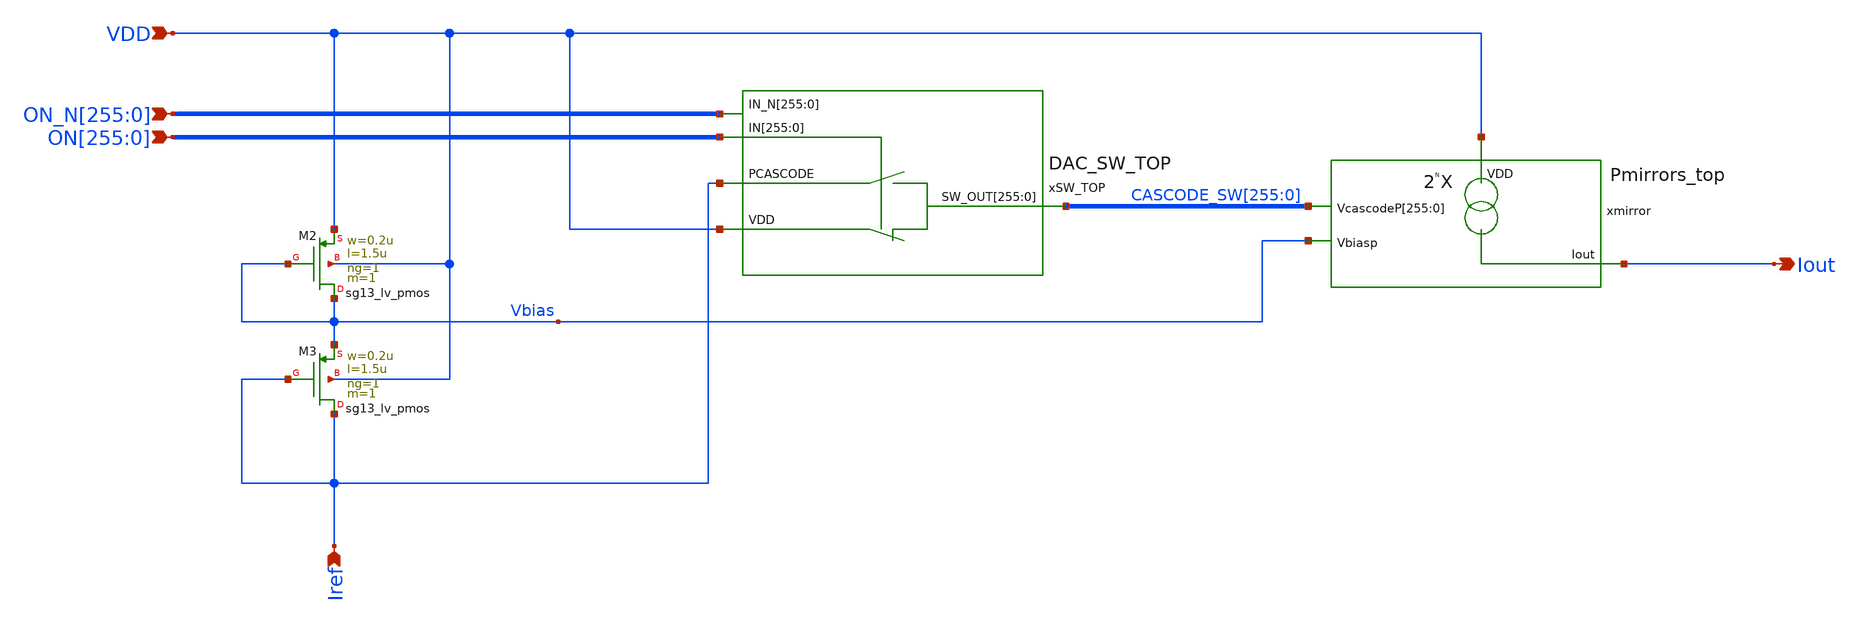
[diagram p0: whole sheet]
** sch_path: schematic/DAC_TOP.sch
**.subckt DAC_TOP VDD Iout
*+ ON[255],ON[254],ON[253],ON[252],ON[251],ON[250],ON[249],ON[248],ON[247],ON[246],ON[245],ON[244],ON[243],ON[242],ON[241],ON[240],ON[239],ON[238],ON[237],ON[236],ON[235],ON[234],ON[233],ON[232],ON[231],ON[230],ON[229],ON[228],ON[227],ON[226],ON[225],ON[224],ON[223],ON[222],ON[221],ON[220],ON[219],ON[218],ON[217],ON[216],ON[215],ON[214],ON[213],ON[212],ON[211],ON[210],ON[209],ON[208],ON[207],ON[206],ON[205],ON[204],ON[203],ON[202],ON[201],ON[200],ON[199],ON[198],ON[197],ON[196],ON[195],ON[194],ON[193],ON[192],ON[191],ON[190],ON[189],ON[188],ON[187],ON[186],ON[185],ON[184],ON[183],ON[182],ON[181],ON[180],ON[179],ON[178],ON[177],ON[176],ON[175],ON[174],ON[173],ON[172],ON[171],ON[170],ON[169],ON[168],ON[167],ON[166],ON[165],ON[164],ON[163],ON[162],ON[161],ON[160],ON[159],ON[158],ON[157],ON[156],ON[155],ON[154],ON[153],ON[152],ON[151],ON[150],ON[149],ON[148],ON[147],ON[146],ON[145],ON[144],ON[143],ON[142],ON[141],ON[140],ON[139],ON[138],ON[137],ON[136],ON[135],ON[134],ON[133],ON[132],ON[131],ON[130],ON[129],ON[128],ON[127],ON[126],ON[125],ON[124],ON[123],ON[122],ON[121],ON[120],ON[119],ON[118],ON[117],ON[116],ON[115],ON[114],ON[113],ON[112],ON[111],ON[110],ON[109],ON[108],ON[107],ON[106],ON[105],ON[104],ON[103],ON[102],ON[101],ON[100],ON[99],ON[98],ON[97],ON[96],ON[95],ON[94],ON[93],ON[92],ON[91],ON[90],ON[89],ON[88],ON[87],ON[86],ON[85],ON[84],ON[83],ON[82],ON[81],ON[80],ON[79],ON[78],ON[77],ON[76],ON[75],ON[74],ON[73],ON[72],ON[71],ON[70],ON[69],ON[68],ON[67],ON[66],ON[65],ON[64],ON[63],ON[62],ON[61],ON[60],ON[59],ON[58],ON[57],ON[56],ON[55],ON[54],ON[53],ON[52],ON[51],ON[50],ON[49],ON[48],ON[47],ON[46],ON[45],ON[44],ON[43],ON[42],ON[41],ON[40],ON[39],ON[38],ON[37],ON[36],ON[35],ON[34],ON[33],ON[32],ON[31],ON[30],ON[29],ON[28],ON[27],ON[26],ON[25],ON[24],ON[23],ON[22],ON[21],ON[20],ON[19],ON[18],ON[17],ON[16],ON[15],ON[14],ON[13],ON[12],ON[11],ON[10],ON[9],ON[8],ON[7],ON[6],ON[5],ON[4],ON[3],ON[2],ON[1],ON[0] Iref
*+ ON_N[255],ON_N[254],ON_N[253],ON_N[252],ON_N[251],ON_N[250],ON_N[249],ON_N[248],ON_N[247],ON_N[246],ON_N[245],ON_N[244],ON_N[243],ON_N[242],ON_N[241],ON_N[240],ON_N[239],ON_N[238],ON_N[237],ON_N[236],ON_N[235],ON_N[234],ON_N[233],ON_N[232],ON_N[231],ON_N[230],ON_N[229],ON_N[228],ON_N[227],ON_N[226],ON_N[225],ON_N[224],ON_N[223],ON_N[222],ON_N[221],ON_N[220],ON_N[219],ON_N[218],ON_N[217],ON_N[216],ON_N[215],ON_N[214],ON_N[213],ON_N[212],ON_N[211],ON_N[210],ON_N[209],ON_N[208],ON_N[207],ON_N[206],ON_N[205],ON_N[204],ON_N[203],ON_N[202],ON_N[201],ON_N[200],ON_N[199],ON_N[198],ON_N[197],ON_N[196],ON_N[195],ON_N[194],ON_N[193],ON_N[192],ON_N[191],ON_N[190],ON_N[189],ON_N[188],ON_N[187],ON_N[186],ON_N[185],ON_N[184],ON_N[183],ON_N[182],ON_N[181],ON_N[180],ON_N[179],ON_N[178],ON_N[177],ON_N[176],ON_N[175],ON_N[174],ON_N[173],ON_N[172],ON_N[171],ON_N[170],ON_N[169],ON_N[168],ON_N[167],ON_N[166],ON_N[165],ON_N[164],ON_N[163],ON_N[162],ON_N[161],ON_N[160],ON_N[159],ON_N[158],ON_N[157],ON_N[156],ON_N[155],ON_N[154],ON_N[153],ON_N[152],ON_N[151],ON_N[150],ON_N[149],ON_N[148],ON_N[147],ON_N[146],ON_N[145],ON_N[144],ON_N[143],ON_N[142],ON_N[141],ON_N[140],ON_N[139],ON_N[138],ON_N[137],ON_N[136],ON_N[135],ON_N[134],ON_N[133],ON_N[132],ON_N[131],ON_N[130],ON_N[129],ON_N[128],ON_N[127],ON_N[126],ON_N[125],ON_N[124],ON_N[123],ON_N[122],ON_N[121],ON_N[120],ON_N[119],ON_N[118],ON_N[117],ON_N[116],ON_N[115],ON_N[114],ON_N[113],ON_N[112],ON_N[111],ON_N[110],ON_N[109],ON_N[108],ON_N[107],ON_N[106],ON_N[105],ON_N[104],ON_N[103],ON_N[102],ON_N[101],ON_N[100],ON_N[99],ON_N[98],ON_N[97],ON_N[96],ON_N[95],ON_N[94],ON_N[93],ON_N[92],ON_N[91],ON_N[90],ON_N[89],ON_N[88],ON_N[87],ON_N[86],ON_N[85],ON_N[84],ON_N[83],ON_N[82],ON_N[81],ON_N[80],ON_N[79],ON_N[78],ON_N[77],ON_N[76],ON_N[75],ON_N[74],ON_N[73],ON_N[72],ON_N[71],ON_N[70],ON_N[69],ON_N[68],ON_N[67],ON_N[66],ON_N[65],ON_N[64],ON_N[63],ON_N[62],ON_N[61],ON_N[60],ON_N[59],ON_N[58],ON_N[57],ON_N[56],ON_N[55],ON_N[54],ON_N[53],ON_N[52],ON_N[51],ON_N[50],ON_N[49],ON_N[48],ON_N[47],ON_N[46],ON_N[45],ON_N[44],ON_N[43],ON_N[42],ON_N[41],ON_N[40],ON_N[39],ON_N[38],ON_N[37],ON_N[36],ON_N[35],ON_N[34],ON_N[33],ON_N[32],ON_N[31],ON_N[30],ON_N[29],ON_N[28],ON_N[27],ON_N[26],ON_N[25],ON_N[24],ON_N[23],ON_N[22],ON_N[21],ON_N[20],ON_N[19],ON_N[18],ON_N[17],ON_N[16],ON_N[15],ON_N[14],ON_N[13],ON_N[12],ON_N[11],ON_N[10],ON_N[9],ON_N[8],ON_N[7],ON_N[6],ON_N[5],ON_N[4],ON_N[3],ON_N[2],ON_N[1],ON_N[0]
*.ipin VDD
*.opin Iout
*.ipin
*+ ON[255],ON[254],ON[253],ON[252],ON[251],ON[250],ON[249],ON[248],ON[247],ON[246],ON[245],ON[244],ON[243],ON[242],ON[241],ON[240],ON[239],ON[238],ON[237],ON[236],ON[235],ON[234],ON[233],ON[232],ON[231],ON[230],ON[229],ON[228],ON[227],ON[226],ON[225],ON[224],ON[223],ON[222],ON[221],ON[220],ON[219],ON[218],ON[217],ON[216],ON[215],ON[214],ON[213],ON[212],ON[211],ON[210],ON[209],ON[208],ON[207],ON[206],ON[205],ON[204],ON[203],ON[202],ON[201],ON[200],ON[199],ON[198],ON[197],ON[196],ON[195],ON[194],ON[193],ON[192],ON[191],ON[190],ON[189],ON[188],ON[187],ON[186],ON[185],ON[184],ON[183],ON[182],ON[181],ON[180],ON[179],ON[178],ON[177],ON[176],ON[175],ON[174],ON[173],ON[172],ON[171],ON[170],ON[169],ON[168],ON[167],ON[166],ON[165],ON[164],ON[163],ON[162],ON[161],ON[160],ON[159],ON[158],ON[157],ON[156],ON[155],ON[154],ON[153],ON[152],ON[151],ON[150],ON[149],ON[148],ON[147],ON[146],ON[145],ON[144],ON[143],ON[142],ON[141],ON[140],ON[139],ON[138],ON[137],ON[136],ON[135],ON[134],ON[133],ON[132],ON[131],ON[130],ON[129],ON[128],ON[127],ON[126],ON[125],ON[124],ON[123],ON[122],ON[121],ON[120],ON[119],ON[118],ON[117],ON[116],ON[115],ON[114],ON[113],ON[112],ON[111],ON[110],ON[109],ON[108],ON[107],ON[106],ON[105],ON[104],ON[103],ON[102],ON[101],ON[100],ON[99],ON[98],ON[97],ON[96],ON[95],ON[94],ON[93],ON[92],ON[91],ON[90],ON[89],ON[88],ON[87],ON[86],ON[85],ON[84],ON[83],ON[82],ON[81],ON[80],ON[79],ON[78],ON[77],ON[76],ON[75],ON[74],ON[73],ON[72],ON[71],ON[70],ON[69],ON[68],ON[67],ON[66],ON[65],ON[64],ON[63],ON[62],ON[61],ON[60],ON[59],ON[58],ON[57],ON[56],ON[55],ON[54],ON[53],ON[52],ON[51],ON[50],ON[49],ON[48],ON[47],ON[46],ON[45],ON[44],ON[43],ON[42],ON[41],ON[40],ON[39],ON[38],ON[37],ON[36],ON[35],ON[34],ON[33],ON[32],ON[31],ON[30],ON[29],ON[28],ON[27],ON[26],ON[25],ON[24],ON[23],ON[22],ON[21],ON[20],ON[19],ON[18],ON[17],ON[16],ON[15],ON[14],ON[13],ON[12],ON[11],ON[10],ON[9],ON[8],ON[7],ON[6],ON[5],ON[4],ON[3],ON[2],ON[1],ON[0]
*.ipin Iref
*.ipin
*+ ON_N[255],ON_N[254],ON_N[253],ON_N[252],ON_N[251],ON_N[250],ON_N[249],ON_N[248],ON_N[247],ON_N[246],ON_N[245],ON_N[244],ON_N[243],ON_N[242],ON_N[241],ON_N[240],ON_N[239],ON_N[238],ON_N[237],ON_N[236],ON_N[235],ON_N[234],ON_N[233],ON_N[232],ON_N[231],ON_N[230],ON_N[229],ON_N[228],ON_N[227],ON_N[226],ON_N[225],ON_N[224],ON_N[223],ON_N[222],ON_N[221],ON_N[220],ON_N[219],ON_N[218],ON_N[217],ON_N[216],ON_N[215],ON_N[214],ON_N[213],ON_N[212],ON_N[211],ON_N[210],ON_N[209],ON_N[208],ON_N[207],ON_N[206],ON_N[205],ON_N[204],ON_N[203],ON_N[202],ON_N[201],ON_N[200],ON_N[199],ON_N[198],ON_N[197],ON_N[196],ON_N[195],ON_N[194],ON_N[193],ON_N[192],ON_N[191],ON_N[190],ON_N[189],ON_N[188],ON_N[187],ON_N[186],ON_N[185],ON_N[184],ON_N[183],ON_N[182],ON_N[181],ON_N[180],ON_N[179],ON_N[178],ON_N[177],ON_N[176],ON_N[175],ON_N[174],ON_N[173],ON_N[172],ON_N[171],ON_N[170],ON_N[169],ON_N[168],ON_N[167],ON_N[166],ON_N[165],ON_N[164],ON_N[163],ON_N[162],ON_N[161],ON_N[160],ON_N[159],ON_N[158],ON_N[157],ON_N[156],ON_N[155],ON_N[154],ON_N[153],ON_N[152],ON_N[151],ON_N[150],ON_N[149],ON_N[148],ON_N[147],ON_N[146],ON_N[145],ON_N[144],ON_N[143],ON_N[142],ON_N[141],ON_N[140],ON_N[139],ON_N[138],ON_N[137],ON_N[136],ON_N[135],ON_N[134],ON_N[133],ON_N[132],ON_N[131],ON_N[130],ON_N[129],ON_N[128],ON_N[127],ON_N[126],ON_N[125],ON_N[124],ON_N[123],ON_N[122],ON_N[121],ON_N[120],ON_N[119],ON_N[118],ON_N[117],ON_N[116],ON_N[115],ON_N[114],ON_N[113],ON_N[112],ON_N[111],ON_N[110],ON_N[109],ON_N[108],ON_N[107],ON_N[106],ON_N[105],ON_N[104],ON_N[103],ON_N[102],ON_N[101],ON_N[100],ON_N[99],ON_N[98],ON_N[97],ON_N[96],ON_N[95],ON_N[94],ON_N[93],ON_N[92],ON_N[91],ON_N[90],ON_N[89],ON_N[88],ON_N[87],ON_N[86],ON_N[85],ON_N[84],ON_N[83],ON_N[82],ON_N[81],ON_N[80],ON_N[79],ON_N[78],ON_N[77],ON_N[76],ON_N[75],ON_N[74],ON_N[73],ON_N[72],ON_N[71],ON_N[70],ON_N[69],ON_N[68],ON_N[67],ON_N[66],ON_N[65],ON_N[64],ON_N[63],ON_N[62],ON_N[61],ON_N[60],ON_N[59],ON_N[58],ON_N[57],ON_N[56],ON_N[55],ON_N[54],ON_N[53],ON_N[52],ON_N[51],ON_N[50],ON_N[49],ON_N[48],ON_N[47],ON_N[46],ON_N[45],ON_N[44],ON_N[43],ON_N[42],ON_N[41],ON_N[40],ON_N[39],ON_N[38],ON_N[37],ON_N[36],ON_N[35],ON_N[34],ON_N[33],ON_N[32],ON_N[31],ON_N[30],ON_N[29],ON_N[28],ON_N[27],ON_N[26],ON_N[25],ON_N[24],ON_N[23],ON_N[22],ON_N[21],ON_N[20],ON_N[19],ON_N[18],ON_N[17],ON_N[16],ON_N[15],ON_N[14],ON_N[13],ON_N[12],ON_N[11],ON_N[10],ON_N[9],ON_N[8],ON_N[7],ON_N[6],ON_N[5],ON_N[4],ON_N[3],ON_N[2],ON_N[1],ON_N[0]
xmirror VDD Iout Vbias CASCODE_SW[255] CASCODE_SW[254] CASCODE_SW[253] CASCODE_SW[252]
+ CASCODE_SW[251] CASCODE_SW[250] CASCODE_SW[249] CASCODE_SW[248] CASCODE_SW[247] CASCODE_SW[246] CASCODE_SW[245]
+ CASCODE_SW[244] CASCODE_SW[243] CASCODE_SW[242] CASCODE_SW[241] CASCODE_SW[240] CASCODE_SW[239] CASCODE_SW[238]
+ CASCODE_SW[237] CASCODE_SW[236] CASCODE_SW[235] CASCODE_SW[234] CASCODE_SW[233] CASCODE_SW[232] CASCODE_SW[231]
+ CASCODE_SW[230] CASCODE_SW[229] CASCODE_SW[228] CASCODE_SW[227] CASCODE_SW[226] CASCODE_SW[225] CASCODE_SW[224]
+ CASCODE_SW[223] CASCODE_SW[222] CASCODE_SW[221] CASCODE_SW[220] CASCODE_SW[219] CASCODE_SW[218] CASCODE_SW[217]
+ CASCODE_SW[216] CASCODE_SW[215] CASCODE_SW[214] CASCODE_SW[213] CASCODE_SW[212] CASCODE_SW[211] CASCODE_SW[210]
+ CASCODE_SW[209] CASCODE_SW[208] CASCODE_SW[207] CASCODE_SW[206] CASCODE_SW[205] CASCODE_SW[204] CASCODE_SW[203]
+ CASCODE_SW[202] CASCODE_SW[201] CASCODE_SW[200] CASCODE_SW[199] CASCODE_SW[198] CASCODE_SW[197] CASCODE_SW[196]
+ CASCODE_SW[195] CASCODE_SW[194] CASCODE_SW[193] CASCODE_SW[192] CASCODE_SW[191] CASCODE_SW[190] CASCODE_SW[189]
+ CASCODE_SW[188] CASCODE_SW[187] CASCODE_SW[186] CASCODE_SW[185] CASCODE_SW[184] CASCODE_SW[183] CASCODE_SW[182]
+ CASCODE_SW[181] CASCODE_SW[180] CASCODE_SW[179] CASCODE_SW[178] CASCODE_SW[177] CASCODE_SW[176] CASCODE_SW[175]
+ CASCODE_SW[174] CASCODE_SW[173] CASCODE_SW[172] CASCODE_SW[171] CASCODE_SW[170] CASCODE_SW[169] CASCODE_SW[168]
+ CASCODE_SW[167] CASCODE_SW[166] CASCODE_SW[165] CASCODE_SW[164] CASCODE_SW[163] CASCODE_SW[162] CASCODE_SW[161]
+ CASCODE_SW[160] CASCODE_SW[159] CASCODE_SW[158] CASCODE_SW[157] CASCODE_SW[156] CASCODE_SW[155] CASCODE_SW[154]
+ CASCODE_SW[153] CASCODE_SW[152] CASCODE_SW[151] CASCODE_SW[150] CASCODE_SW[149] CASCODE_SW[148] CASCODE_SW[147]
+ CASCODE_SW[146] CASCODE_SW[145] CASCODE_SW[144] CASCODE_SW[143] CASCODE_SW[142] CASCODE_SW[141] CASCODE_SW[140]
+ CASCODE_SW[139] CASCODE_SW[138] CASCODE_SW[137] CASCODE_SW[136] CASCODE_SW[135] CASCODE_SW[134] CASCODE_SW[133]
+ CASCODE_SW[132] CASCODE_SW[131] CASCODE_SW[130] CASCODE_SW[129] CASCODE_SW[128] CASCODE_SW[127] CASCODE_SW[126]
+ CASCODE_SW[125] CASCODE_SW[124] CASCODE_SW[123] CASCODE_SW[122] CASCODE_SW[121] CASCODE_SW[120] CASCODE_SW[119]
+ CASCODE_SW[118] CASCODE_SW[117] CASCODE_SW[116] CASCODE_SW[115] CASCODE_SW[114] CASCODE_SW[113] CASCODE_SW[112]
+ CASCODE_SW[111] CASCODE_SW[110] CASCODE_SW[109] CASCODE_SW[108] CASCODE_SW[107] CASCODE_SW[106] CASCODE_SW[105]
+ CASCODE_SW[104] CASCODE_SW[103] CASCODE_SW[102] CASCODE_SW[101] CASCODE_SW[100] CASCODE_SW[99] CASCODE_SW[98]
+ CASCODE_SW[97] CASCODE_SW[96] CASCODE_SW[95] CASCODE_SW[94] CASCODE_SW[93] CASCODE_SW[92] CASCODE_SW[91]
+ CASCODE_SW[90] CASCODE_SW[89] CASCODE_SW[88] CASCODE_SW[87] CASCODE_SW[86] CASCODE_SW[85] CASCODE_SW[84]
+ CASCODE_SW[83] CASCODE_SW[82] CASCODE_SW[81] CASCODE_SW[80] CASCODE_SW[79] CASCODE_SW[78] CASCODE_SW[77]
+ CASCODE_SW[76] CASCODE_SW[75] CASCODE_SW[74] CASCODE_SW[73] CASCODE_SW[72] CASCODE_SW[71] CASCODE_SW[70]
+ CASCODE_SW[69] CASCODE_SW[68] CASCODE_SW[67] CASCODE_SW[66] CASCODE_SW[65] CASCODE_SW[64] CASCODE_SW[63]
+ CASCODE_SW[62] CASCODE_SW[61] CASCODE_SW[60] CASCODE_SW[59] CASCODE_SW[58] CASCODE_SW[57] CASCODE_SW[56]
+ CASCODE_SW[55] CASCODE_SW[54] CASCODE_SW[53] CASCODE_SW[52] CASCODE_SW[51] CASCODE_SW[50] CASCODE_SW[49]
+ CASCODE_SW[48] CASCODE_SW[47] CASCODE_SW[46] CASCODE_SW[45] CASCODE_SW[44] CASCODE_SW[43] CASCODE_SW[42]
+ CASCODE_SW[41] CASCODE_SW[40] CASCODE_SW[39] CASCODE_SW[38] CASCODE_SW[37] CASCODE_SW[36] CASCODE_SW[35]
+ CASCODE_SW[34] CASCODE_SW[33] CASCODE_SW[32] CASCODE_SW[31] CASCODE_SW[30] CASCODE_SW[29] CASCODE_SW[28]
+ CASCODE_SW[27] CASCODE_SW[26] CASCODE_SW[25] CASCODE_SW[24] CASCODE_SW[23] CASCODE_SW[22] CASCODE_SW[21]
+ CASCODE_SW[20] CASCODE_SW[19] CASCODE_SW[18] CASCODE_SW[17] CASCODE_SW[16] CASCODE_SW[15] CASCODE_SW[14]
+ CASCODE_SW[13] CASCODE_SW[12] CASCODE_SW[11] CASCODE_SW[10] CASCODE_SW[9] CASCODE_SW[8] CASCODE_SW[7]
+ CASCODE_SW[6] CASCODE_SW[5] CASCODE_SW[4] CASCODE_SW[3] CASCODE_SW[2] CASCODE_SW[1] CASCODE_SW[0] Pmirrors_top
XM2 Vbias Vbias VDD VDD sg13_lv_pmos w=0.2u l=1.5u ng=1 m=1 mm_ok=1
XM3 Iref Iref Vbias VDD sg13_lv_pmos w=0.2u l=1.5u ng=1 m=1 mm_ok=1
xSW_TOP Iref CASCODE_SW[255] CASCODE_SW[254] CASCODE_SW[253] CASCODE_SW[252] CASCODE_SW[251]
+ CASCODE_SW[250] CASCODE_SW[249] CASCODE_SW[248] CASCODE_SW[247] CASCODE_SW[246] CASCODE_SW[245] CASCODE_SW[244]
+ CASCODE_SW[243] CASCODE_SW[242] CASCODE_SW[241] CASCODE_SW[240] CASCODE_SW[239] CASCODE_SW[238] CASCODE_SW[237]
+ CASCODE_SW[236] CASCODE_SW[235] CASCODE_SW[234] CASCODE_SW[233] CASCODE_SW[232] CASCODE_SW[231] CASCODE_SW[230]
+ CASCODE_SW[229] CASCODE_SW[228] CASCODE_SW[227] CASCODE_SW[226] CASCODE_SW[225] CASCODE_SW[224] CASCODE_SW[223]
+ CASCODE_SW[222] CASCODE_SW[221] CASCODE_SW[220] CASCODE_SW[219] CASCODE_SW[218] CASCODE_SW[217] CASCODE_SW[216]
+ CASCODE_SW[215] CASCODE_SW[214] CASCODE_SW[213] CASCODE_SW[212] CASCODE_SW[211] CASCODE_SW[210] CASCODE_SW[209]
+ CASCODE_SW[208] CASCODE_SW[207] CASCODE_SW[206] CASCODE_SW[205] CASCODE_SW[204] CASCODE_SW[203] CASCODE_SW[202]
+ CASCODE_SW[201] CASCODE_SW[200] CASCODE_SW[199] CASCODE_SW[198] CASCODE_SW[197] CASCODE_SW[196] CASCODE_SW[195]
+ CASCODE_SW[194] CASCODE_SW[193] CASCODE_SW[192] CASCODE_SW[191] CASCODE_SW[190] CASCODE_SW[189] CASCODE_SW[188]
+ CASCODE_SW[187] CASCODE_SW[186] CASCODE_SW[185] CASCODE_SW[184] CASCODE_SW[183] CASCODE_SW[182] CASCODE_SW[181]
+ CASCODE_SW[180] CASCODE_SW[179] CASCODE_SW[178] CASCODE_SW[177] CASCODE_SW[176] CASCODE_SW[175] CASCODE_SW[174]
+ CASCODE_SW[173] CASCODE_SW[172] CASCODE_SW[171] CASCODE_SW[170] CASCODE_SW[169] CASCODE_SW[168] CASCODE_SW[167]
+ CASCODE_SW[166] CASCODE_SW[165] CASCODE_SW[164] CASCODE_SW[163] CASCODE_SW[162] CASCODE_SW[161] CASCODE_SW[160]
+ CASCODE_SW[159] CASCODE_SW[158] CASCODE_SW[157] CASCODE_SW[156] CASCODE_SW[155] CASCODE_SW[154] CASCODE_SW[153]
+ CASCODE_SW[152] CASCODE_SW[151] CASCODE_SW[150] CASCODE_SW[149] CASCODE_SW[148] CASCODE_SW[147] CASCODE_SW[146]
+ CASCODE_SW[145] CASCODE_SW[144] CASCODE_SW[143] CASCODE_SW[142] CASCODE_SW[141] CASCODE_SW[140] CASCODE_SW[139]
+ CASCODE_SW[138] CASCODE_SW[137] CASCODE_SW[136] CASCODE_SW[135] CASCODE_SW[134] CASCODE_SW[133] CASCODE_SW[132]
+ CASCODE_SW[131] CASCODE_SW[130] CASCODE_SW[129] CASCODE_SW[128] CASCODE_SW[127] CASCODE_SW[126] CASCODE_SW[125]
+ CASCODE_SW[124] CASCODE_SW[123] CASCODE_SW[122] CASCODE_SW[121] CASCODE_SW[120] CASCODE_SW[119] CASCODE_SW[118]
+ CASCODE_SW[117] CASCODE_SW[116] CASCODE_SW[115] CASCODE_SW[114] CASCODE_SW[113] CASCODE_SW[112] CASCODE_SW[111]
+ CASCODE_SW[110] CASCODE_SW[109] CASCODE_SW[108] CASCODE_SW[107] CASCODE_SW[106] CASCODE_SW[105] CASCODE_SW[104]
+ CASCODE_SW[103] CASCODE_SW[102] CASCODE_SW[101] CASCODE_SW[100] CASCODE_SW[99] CASCODE_SW[98] CASCODE_SW[97]
+ CASCODE_SW[96] CASCODE_SW[95] CASCODE_SW[94] CASCODE_SW[93] CASCODE_SW[92] CASCODE_SW[91] CASCODE_SW[90]
+ CASCODE_SW[89] CASCODE_SW[88] CASCODE_SW[87] CASCODE_SW[86] CASCODE_SW[85] CASCODE_SW[84] CASCODE_SW[83]
+ CASCODE_SW[82] CASCODE_SW[81] CASCODE_SW[80] CASCODE_SW[79] CASCODE_SW[78] CASCODE_SW[77] CASCODE_SW[76]
+ CASCODE_SW[75] CASCODE_SW[74] CASCODE_SW[73] CASCODE_SW[72] CASCODE_SW[71] CASCODE_SW[70] CASCODE_SW[69]
+ CASCODE_SW[68] CASCODE_SW[67] CASCODE_SW[66] CASCODE_SW[65] CASCODE_SW[64] CASCODE_SW[63] CASCODE_SW[62]
+ CASCODE_SW[61] CASCODE_SW[60] CASCODE_SW[59] CASCODE_SW[58] CASCODE_SW[57] CASCODE_SW[56] CASCODE_SW[55]
+ CASCODE_SW[54] CASCODE_SW[53] CASCODE_SW[52] CASCODE_SW[51] CASCODE_SW[50] CASCODE_SW[49] CASCODE_SW[48]
+ CASCODE_SW[47] CASCODE_SW[46] CASCODE_SW[45] CASCODE_SW[44] CASCODE_SW[43] CASCODE_SW[42] CASCODE_SW[41]
+ CASCODE_SW[40] CASCODE_SW[39] CASCODE_SW[38] CASCODE_SW[37] CASCODE_SW[36] CASCODE_SW[35] CASCODE_SW[34]
+ CASCODE_SW[33] CASCODE_SW[32] CASCODE_SW[31] CASCODE_SW[30] CASCODE_SW[29] CASCODE_SW[28] CASCODE_SW[27]
+ CASCODE_SW[26] CASCODE_SW[25] CASCODE_SW[24] CASCODE_SW[23] CASCODE_SW[22] CASCODE_SW[21] CASCODE_SW[20]
+ CASCODE_SW[19] CASCODE_SW[18] CASCODE_SW[17] CASCODE_SW[16] CASCODE_SW[15] CASCODE_SW[14] CASCODE_SW[13]
+ CASCODE_SW[12] CASCODE_SW[11] CASCODE_SW[10] CASCODE_SW[9] CASCODE_SW[8] CASCODE_SW[7] CASCODE_SW[6] CASCODE_SW[5]
+ CASCODE_SW[4] CASCODE_SW[3] CASCODE_SW[2] CASCODE_SW[1] CASCODE_SW[0] VDD ON[255] ON[254] ON[253] ON[252] ON[251]
+ ON[250] ON[249] ON[248] ON[247] ON[246] ON[245] ON[244] ON[243] ON[242] ON[241] ON[240] ON[239] ON[238]
+ ON[237] ON[236] ON[235] ON[234] ON[233] ON[232] ON[231] ON[230] ON[229] ON[228] ON[227] ON[226] ON[225]
+ ON[224] ON[223] ON[222] ON[221] ON[220] ON[219] ON[218] ON[217] ON[216] ON[215] ON[214] ON[213] ON[212]
+ ON[211] ON[210] ON[209] ON[208] ON[207] ON[206] ON[205] ON[204] ON[203] ON[202] ON[201] ON[200] ON[199]
+ ON[198] ON[197] ON[196] ON[195] ON[194] ON[193] ON[192] ON[191] ON[190] ON[189] ON[188] ON[187] ON[186]
+ ON[185] ON[184] ON[183] ON[182] ON[181] ON[180] ON[179] ON[178] ON[177] ON[176] ON[175] ON[174] ON[173]
+ ON[172] ON[171] ON[170] ON[169] ON[168] ON[167] ON[166] ON[165] ON[164] ON[163] ON[162] ON[161] ON[160]
+ ON[159] ON[158] ON[157] ON[156] ON[155] ON[154] ON[153] ON[152] ON[151] ON[150] ON[149] ON[148] ON[147]
+ ON[146] ON[145] ON[144] ON[143] ON[142] ON[141] ON[140] ON[139] ON[138] ON[137] ON[136] ON[135] ON[134]
+ ON[133] ON[132] ON[131] ON[130] ON[129] ON[128] ON[127] ON[126] ON[125] ON[124] ON[123] ON[122] ON[121]
+ ON[120] ON[119] ON[118] ON[117] ON[116] ON[115] ON[114] ON[113] ON[112] ON[111] ON[110] ON[109] ON[108]
+ ON[107] ON[106] ON[105] ON[104] ON[103] ON[102] ON[101] ON[100] ON[99] ON[98] ON[97] ON[96] ON[95] ON[94]
+ ON[93] ON[92] ON[91] ON[90] ON[89] ON[88] ON[87] ON[86] ON[85] ON[84] ON[83] ON[82] ON[81] ON[80] ON[79]
+ ON[78] ON[77] ON[76] ON[75] ON[74] ON[73] ON[72] ON[71] ON[70] ON[69] ON[68] ON[67] ON[66] ON[65] ON[64]
+ ON[63] ON[62] ON[61] ON[60] ON[59] ON[58] ON[57] ON[56] ON[55] ON[54] ON[53] ON[52] ON[51] ON[50] ON[49]
+ ON[48] ON[47] ON[46] ON[45] ON[44] ON[43] ON[42] ON[41] ON[40] ON[39] ON[38] ON[37] ON[36] ON[35] ON[34]
+ ON[33] ON[32] ON[31] ON[30] ON[29] ON[28] ON[27] ON[26] ON[25] ON[24] ON[23] ON[22] ON[21] ON[20] ON[19]
+ ON[18] ON[17] ON[16] ON[15] ON[14] ON[13] ON[12] ON[11] ON[10] ON[9] ON[8] ON[7] ON[6] ON[5] ON[4] ON[3]
+ ON[2] ON[1] ON[0] ON_N[255] ON_N[254] ON_N[253] ON_N[252] ON_N[251] ON_N[250] ON_N[249] ON_N[248]
+ ON_N[247] ON_N[246] ON_N[245] ON_N[244] ON_N[243] ON_N[242] ON_N[241] ON_N[240] ON_N[239] ON_N[238] ON_N[237]
+ ON_N[236] ON_N[235] ON_N[234] ON_N[233] ON_N[232] ON_N[231] ON_N[230] ON_N[229] ON_N[228] ON_N[227] ON_N[226]
+ ON_N[225] ON_N[224] ON_N[223] ON_N[222] ON_N[221] ON_N[220] ON_N[219] ON_N[218] ON_N[217] ON_N[216] ON_N[215]
+ ON_N[214] ON_N[213] ON_N[212] ON_N[211] ON_N[210] ON_N[209] ON_N[208] ON_N[207] ON_N[206] ON_N[205] ON_N[204]
+ ON_N[203] ON_N[202] ON_N[201] ON_N[200] ON_N[199] ON_N[198] ON_N[197] ON_N[196] ON_N[195] ON_N[194] ON_N[193]
+ ON_N[192] ON_N[191] ON_N[190] ON_N[189] ON_N[188] ON_N[187] ON_N[186] ON_N[185] ON_N[184] ON_N[183] ON_N[182]
+ ON_N[181] ON_N[180] ON_N[179] ON_N[178] ON_N[177] ON_N[176] ON_N[175] ON_N[174] ON_N[173] ON_N[172] ON_N[171]
+ ON_N[170] ON_N[169] ON_N[168] ON_N[167] ON_N[166] ON_N[165] ON_N[164] ON_N[163] ON_N[162] ON_N[161] ON_N[160]
+ ON_N[159] ON_N[158] ON_N[157] ON_N[156] ON_N[155] ON_N[154] ON_N[153] ON_N[152] ON_N[151] ON_N[150] ON_N[149]
+ ON_N[148] ON_N[147] ON_N[146] ON_N[145] ON_N[144] ON_N[143] ON_N[142] ON_N[141] ON_N[140] ON_N[139] ON_N[138]
+ ON_N[137] ON_N[136] ON_N[135] ON_N[134] ON_N[133] ON_N[132] ON_N[131] ON_N[130] ON_N[129] ON_N[128] ON_N[127]
+ ON_N[126] ON_N[125] ON_N[124] ON_N[123] ON_N[122] ON_N[121] ON_N[120] ON_N[119] ON_N[118] ON_N[117] ON_N[116]
+ ON_N[115] ON_N[114] ON_N[113] ON_N[112] ON_N[111] ON_N[110] ON_N[109] ON_N[108] ON_N[107] ON_N[106] ON_N[105]
+ ON_N[104] ON_N[103] ON_N[102] ON_N[101] ON_N[100] ON_N[99] ON_N[98] ON_N[97] ON_N[96] ON_N[95] ON_N[94]
+ ON_N[93] ON_N[92] ON_N[91] ON_N[90] ON_N[89] ON_N[88] ON_N[87] ON_N[86] ON_N[85] ON_N[84] ON_N[83] ON_N[82]
+ ON_N[81] ON_N[80] ON_N[79] ON_N[78] ON_N[77] ON_N[76] ON_N[75] ON_N[74] ON_N[73] ON_N[72] ON_N[71] ON_N[70]
+ ON_N[69] ON_N[68] ON_N[67] ON_N[66] ON_N[65] ON_N[64] ON_N[63] ON_N[62] ON_N[61] ON_N[60] ON_N[59] ON_N[58]
+ ON_N[57] ON_N[56] ON_N[55] ON_N[54] ON_N[53] ON_N[52] ON_N[51] ON_N[50] ON_N[49] ON_N[48] ON_N[47] ON_N[46]
+ ON_N[45] ON_N[44] ON_N[43] ON_N[42] ON_N[41] ON_N[40] ON_N[39] ON_N[38] ON_N[37] ON_N[36] ON_N[35] ON_N[34]
+ ON_N[33] ON_N[32] ON_N[31] ON_N[30] ON_N[29] ON_N[28] ON_N[27] ON_N[26] ON_N[25] ON_N[24] ON_N[23] ON_N[22]
+ ON_N[21] ON_N[20] ON_N[19] ON_N[18] ON_N[17] ON_N[16] ON_N[15] ON_N[14] ON_N[13] ON_N[12] ON_N[11] ON_N[10]
+ ON_N[9] ON_N[8] ON_N[7] ON_N[6] ON_N[5] ON_N[4] ON_N[3] ON_N[2] ON_N[1] ON_N[0] DAC_SW_TOP
**.ends
.end
